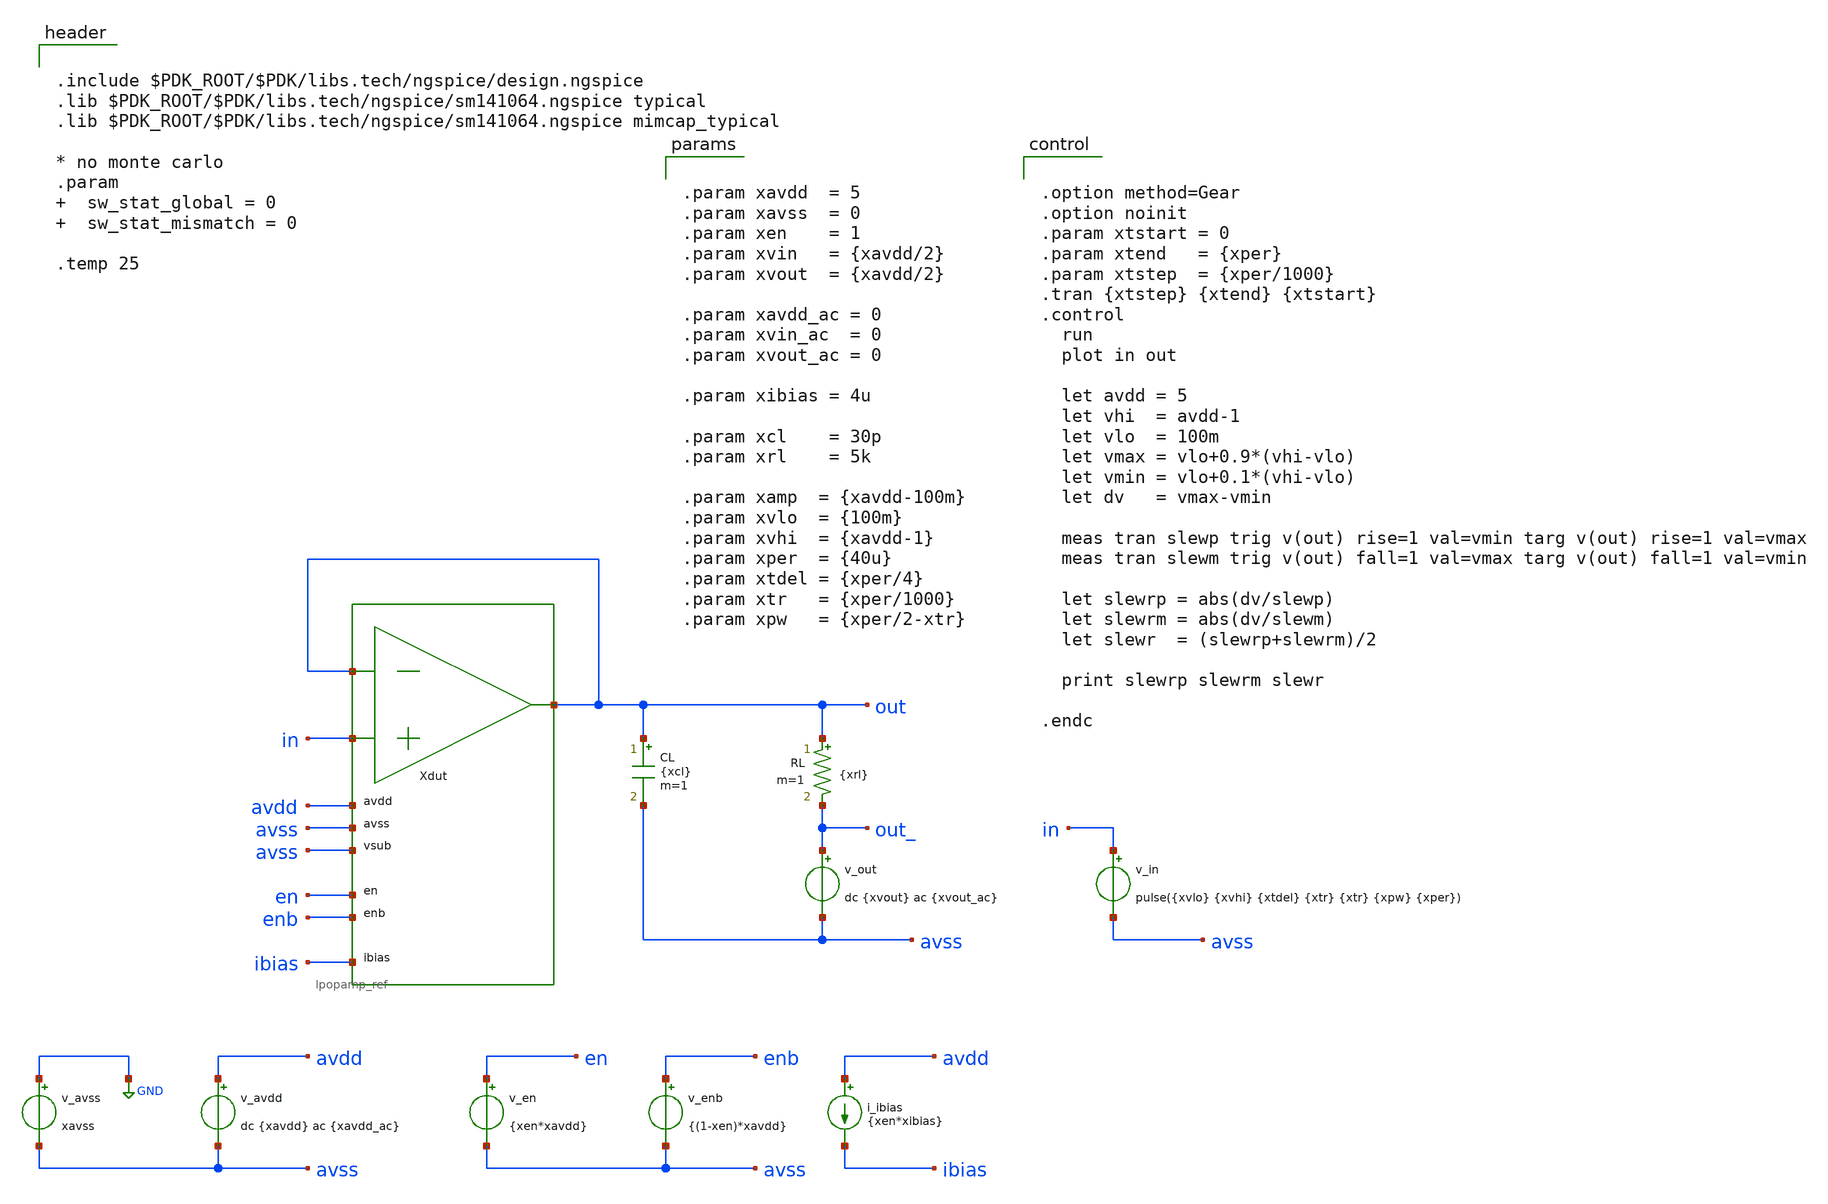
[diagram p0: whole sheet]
** sch_path: xschem/tb_lpopamp_buf_tran_step_large.sch
**.subckt tb_lpopamp_buf_tran_step_large
Xdut out in out avdd avss avss en enb ibias lpopamp_ref
v_avss GND avss xavss
v_avdd avdd avss dc {xavdd} ac {xavdd_ac}
v_in in avss pulse({xvlo} {xvhi} {xtdel} {xtr} {xtr} {xpw} {xper})
v_en en avss {xen*xavdd}
v_enb enb avss {(1-xen)*xavdd}
i_ibias avdd ibias {xen*xibias}
CL out avss {xcl} m=1
v_out out_ avss dc {xvout} ac {xvout_ac}
RL out out_ {xrl} m=1
**** begin user architecture code


.include $PDK_ROOT/$PDK/libs.tech/ngspice/design.ngspice
.lib $PDK_ROOT/$PDK/libs.tech/ngspice/sm141064.ngspice typical
.lib $PDK_ROOT/$PDK/libs.tech/ngspice/sm141064.ngspice mimcap_typical

* no monte carlo
.param   sw_stat_global = 0   sw_stat_mismatch = 0

.temp 25




.option method=Gear
.option noinit
.param xtstart = 0
.param xtend   = {xper}
.param xtstep  = {xper/1000}
.tran {xtstep} {xtend} {xtstart}
.control
  run
  plot in out

  let avdd = 5
  let vhi  = avdd-1
  let vlo  = 100m
  let vmax = vlo+0.9*(vhi-vlo)
  let vmin = vlo+0.1*(vhi-vlo)
  let dv   = vmax-vmin

  meas tran slewp trig v(out) rise=1 val=vmin targ v(out) rise=1 val=vmax
  meas tran slewm trig v(out) fall=1 val=vmax targ v(out) fall=1 val=vmin

  let slewrp = abs(dv/slewp)
  let slewrm = abs(dv/slewm)
  let slewr  = (slewrp+slewrm)/2

  print slewrp slewrm slewr

.endc




.param xavdd  = 5
.param xavss  = 0
.param xen    = 1
.param xvin   = {xavdd/2}
.param xvout  = {xavdd/2}

.param xavdd_ac = 0
.param xvin_ac  = 0
.param xvout_ac = 0

.param xibias = 4u

.param xcl    = 30p
.param xrl    = 5k

.param xamp  = {xavdd-100m}
.param xvlo  = {100m}
.param xvhi  = {xavdd-1}
.param xper  = {40u}
.param xtdel = {xper/4}
.param xtr   = {xper/1000}
.param xpw   = {xper/2-xtr}


**** end user architecture code
**.ends
.GLOBAL GND
.end
